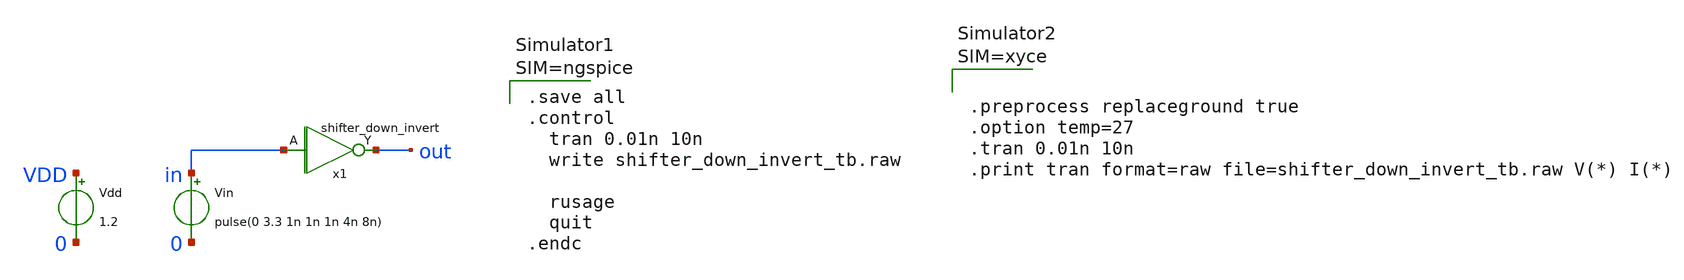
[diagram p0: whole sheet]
** sch_path: FLDO/design_data/xschem/shifter_down_invert_tb.sch
**.subckt shifter_down_invert_tb
x1 out in VDD 0 shifter_down_invert
Vdd VDD 0 1.2
Vin in 0 pulse(0 3.3 1n 1n 1n 4n 8n)
**** begin user architecture code



** IHP models
.lib cornerMOSlv.lib mos_tt
.lib cornerMOShv.lib mos_tt
.lib cornerHBT.lib hbt_typ
.lib cornerRES.lib res_typ
.lib cornerCAP.lib cap_typ

.include sg13g2_stdcell.spice






.save all
.control
  tran 0.01n 10n
  write shifter_down_invert_tb.raw

  rusage
  quit
.endc









**** end user architecture code
**.ends

* expanding   symbol:  shifter_down_invert.sym # of pins=2
** sym_path: FLDO/design_data/xschem/shifter_down_invert.sym
** sch_path: FLDO/design_data/xschem/shifter_down_invert.sch
.subckt shifter_down_invert Y A VDD VSS
*.opin Y
*.ipin A
XM1 Y A VSS VSS sg13_hv_nmos w=0.3u l=0.45u ng=1 m=1 mm_ok=1
XM2 Y A VDD VDD sg13_hv_pmos w=0.3u l=0.4u ng=1 m=1 mm_ok=1
.ends

.end
